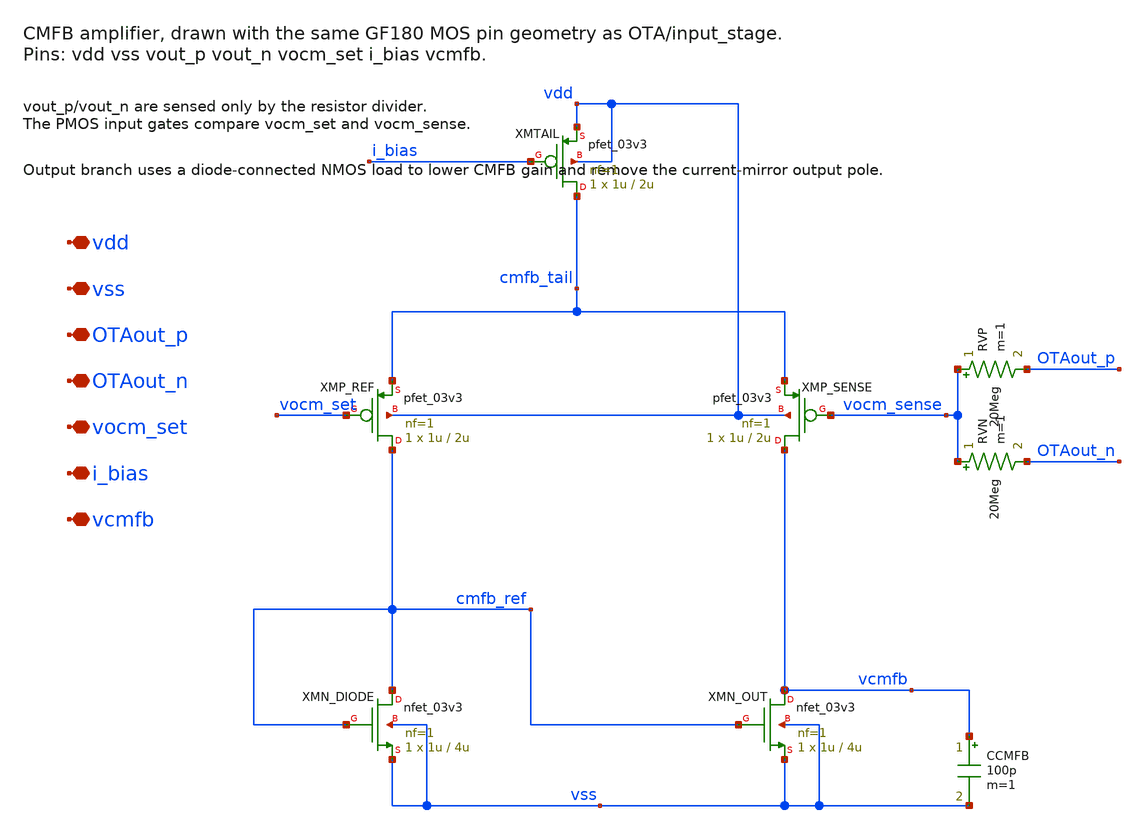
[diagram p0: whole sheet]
** sch_path: CMFB.sch
**.subckt CMFB vdd vss OTAout_p OTAout_n vocm_set i_bias vcmfb
*.iopin vdd
*.iopin vss
*.iopin OTAout_p
*.iopin OTAout_n
*.iopin vocm_set
*.iopin i_bias
*.iopin vcmfb
XMTAIL cmfb_tail i_bias vdd vdd pfet_03v3 L=2u W=1u nf=1 ad='int((nf+1)/2) * W/nf * 0.18u' as='int((nf+2)/2) * W/nf * 0.18u'
+ pd='2*int((nf+1)/2) * (W/nf + 0.18u)' ps='2*int((nf+2)/2) * (W/nf + 0.18u)' nrd='0.18u / W' nrs='0.18u / W'
+ sa=0 sb=0 sd=0 m=1
XMP_REF cmfb_ref vocm_set cmfb_tail vdd pfet_03v3 L=2u W=1u nf=1 ad='int((nf+1)/2) * W/nf * 0.18u' as='int((nf+2)/2) * W/nf * 0.18u'
+ pd='2*int((nf+1)/2) * (W/nf + 0.18u)' ps='2*int((nf+2)/2) * (W/nf + 0.18u)' nrd='0.18u / W' nrs='0.18u / W'
+ sa=0 sb=0 sd=0 m=1
XMP_SENSE vcmfb vocm_sense cmfb_tail vdd pfet_03v3 L=2u W=1u nf=1 ad='int((nf+1)/2) * W/nf * 0.18u' as='int((nf+2)/2) * W/nf * 0.18u'
+ pd='2*int((nf+1)/2) * (W/nf + 0.18u)' ps='2*int((nf+2)/2) * (W/nf + 0.18u)' nrd='0.18u / W' nrs='0.18u / W'
+ sa=0 sb=0 sd=0 m=1
XMN_DIODE cmfb_ref cmfb_ref vss vss nfet_03v3 L=4u W=1u nf=1 ad='int((nf+1)/2) * W/nf * 0.18u' as='int((nf+2)/2) * W/nf * 0.18u'
+ pd='2*int((nf+1)/2) * (W/nf + 0.18u)' ps='2*int((nf+2)/2) * (W/nf + 0.18u)' nrd='0.18u / W' nrs='0.18u / W'
+ sa=0 sb=0 sd=0 m=1
XMN_OUT vcmfb cmfb_ref vss vss nfet_03v3 L=4u W=1u nf=1 ad='int((nf+1)/2) * W/nf * 0.18u' as='int((nf+2)/2) * W/nf * 0.18u'
+ pd='2*int((nf+1)/2) * (W/nf + 0.18u)' ps='2*int((nf+2)/2) * (W/nf + 0.18u)' nrd='0.18u / W' nrs='0.18u / W'
+ sa=0 sb=0 sd=0 m=1
RVP vocm_sense OTAout_p 20Meg m=1
RVN vocm_sense OTAout_n 20Meg m=1
CCMFB vcmfb vss 100p m=1
**.ends
.end
